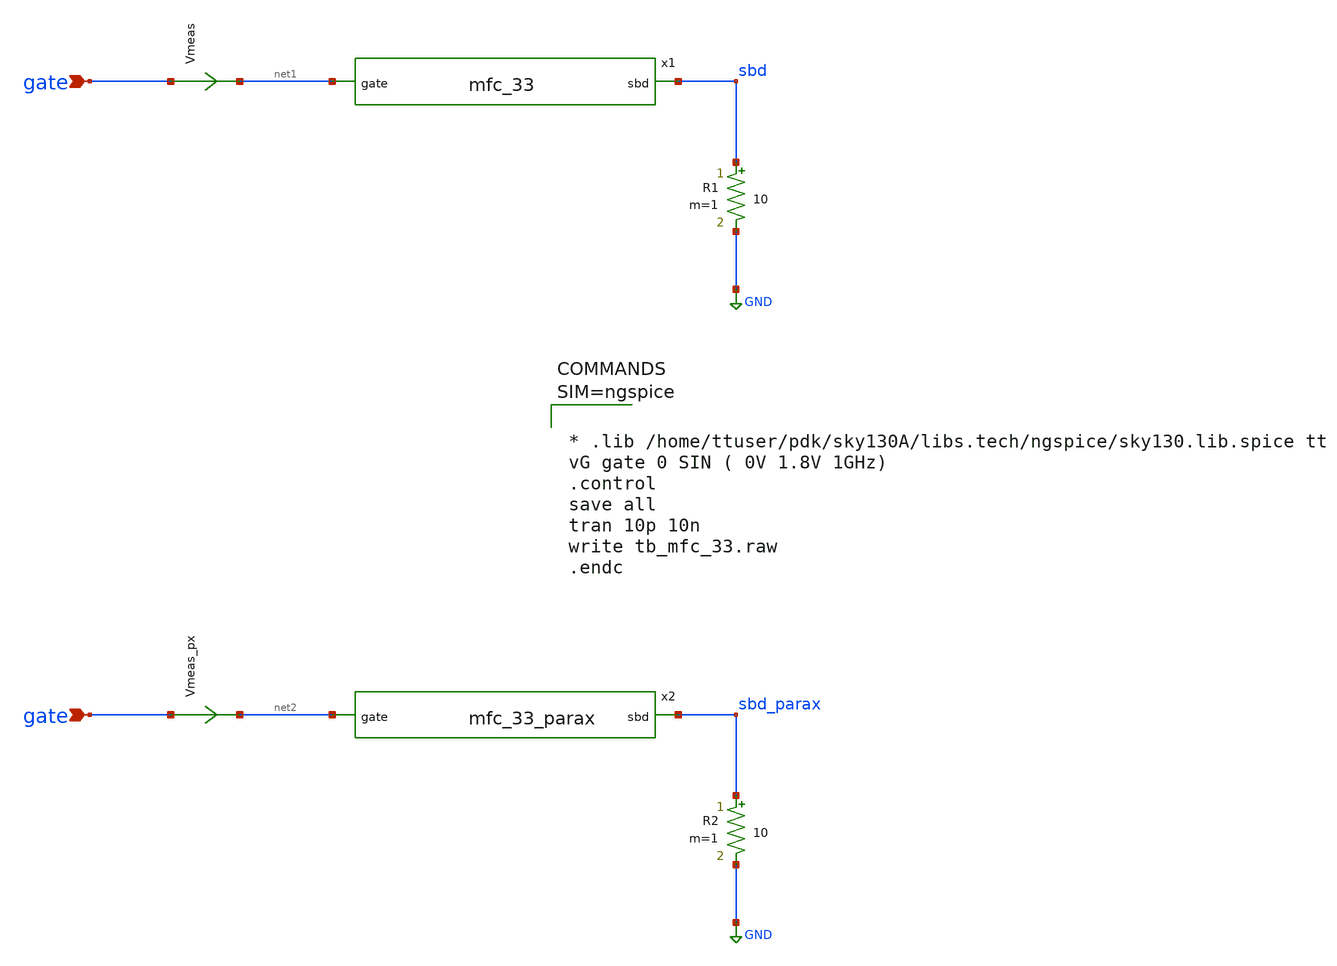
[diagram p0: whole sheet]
** sch_path: xschem/tb_mfc_33.sch
**.subckt tb_mfc_33 gate gate
*.ipin gate
*.ipin gate
Vmeas gate net1 0
.save i(vmeas)
R1 sbd GND 10 m=1
x1 net1 sbd mfc_33
Vmeas_px gate net2 0
.save i(vmeas_px)
R2 sbd_parax GND 10 m=1
x2 net2 sbd_parax mfc_33_parax
**** begin user architecture code

** opencircuitdesign pdks install
.lib $::SKYWATER_MODELS/sky130.lib.spice tt





* .lib /home/ttuser/pdk/sky130A/libs.tech/ngspice/sky130.lib.spice tt
vG gate 0 SIN ( 0V 1.8V 1GHz)
.control
save all
tran 10p 10n
write tb_mfc_33.raw
.endc



**** end user architecture code
**.ends

* expanding   symbol:  mfc_33.sym # of pins=2
** sym_path: xschem/mfc_33.sym
** sch_path: xschem/mfc_33.sch
.subckt mfc_33 gate sbd
*.ipin gate
*.opin sbd
XM2 sbd gate sbd sbd sky130_fd_pr__nfet_01v8 L=1.2 W=3.36 nf=1 ad='int((nf+1)/2) * W/nf * 0.29' as='int((nf+2)/2) * W/nf * 0.29'
+ pd='2*int((nf+1)/2) * (W/nf + 0.29)' ps='2*int((nf+2)/2) * (W/nf + 0.29)' nrd='0.29 / W' nrs='0.29 / W'
+ sa=0 sb=0 sd=0 mult=1 m=1
.ends


* expanding   symbol:  mfc_33_parax.sym # of pins=2
** sym_path: xschem/mfc_33.sym
.include [file normalize ../mag/mfc_33.sim.spice]
.GLOBAL GND
.end
